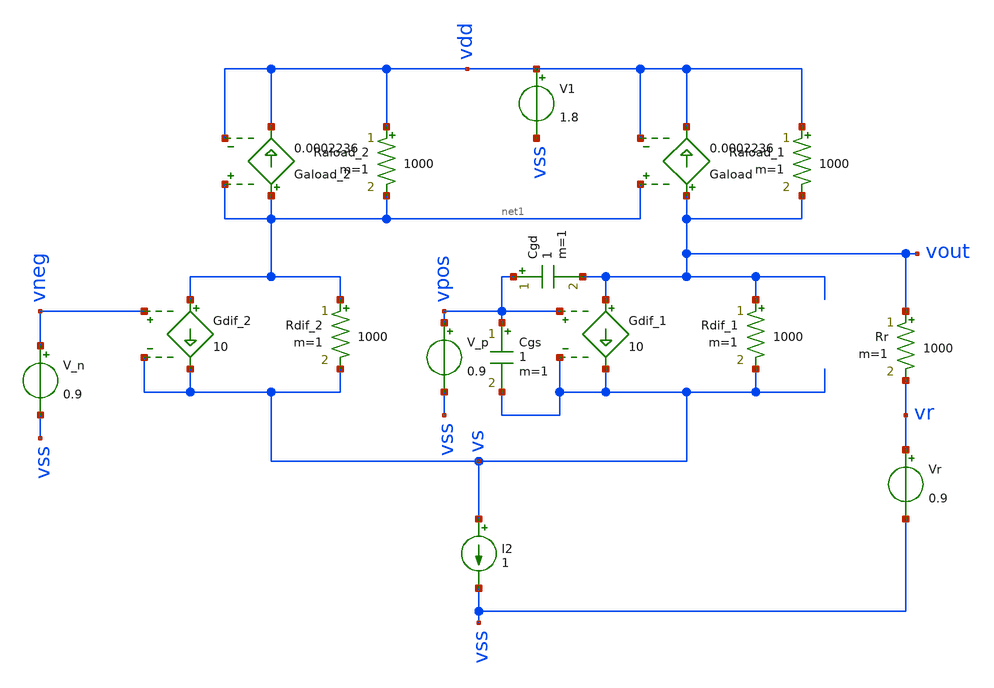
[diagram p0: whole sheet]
** sch_path: test/sstadex/xschem/ota_cap_r.sch
**.subckt ota_cap_r
Rdif_2 net1 vs 1000 m=1
Gdif_2 net1 vs vneg vs 10
Rdif_1 vout vs 1000 m=1
Gdif_1 vout vs vpos vs 10
I2 vs vss 1
V1 vdd vss 1.8
V_n vneg vss 0.9
V_p vpos vss 0.9
Raload_1 vdd vout 1000 m=1
Raload_2 vdd net1 1000 m=1
Gaload vout vdd net1 vdd 0.0002236
Cgd vpos vout 1 m=1
Cgs vpos vs 1 m=1
Vr vr vss 0.9
Rr vout vr 1000 m=1
Gaload_2 net1 vdd net1 vdd 0.0002236
**.ends
.end
